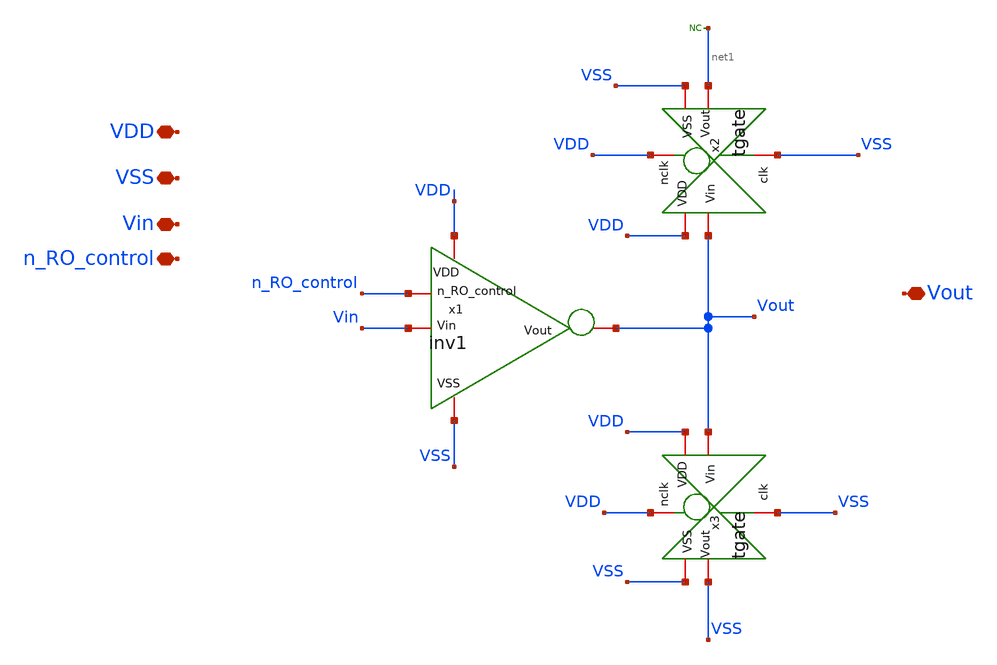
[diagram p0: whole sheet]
** sch_path: TT/rovcel4.sch
**.subckt rovcel4 VDD VSS Vin n_RO_control Vout
*.iopin VDD
*.iopin VSS
*.iopin Vin
*.iopin n_RO_control
*.iopin Vout
x1 n_RO_control VDD VSS Vin Vout inv1
x2 VDD VDD Vout net1 VSS VSS tgate
x3 VDD VDD Vout VSS VSS VSS tgate
* noconn #net1
**.ends

* expanding   symbol:  /foss/designs/Projects/RO_reliability/xschem/inv1.sym # of pins=5
** sym_path: TT/inv1.sym
** sch_path: TT/inv1.sch
.subckt inv1 n_RO_control VDD VSS Vin Vout
*.iopin VDD
*.iopin VSS
*.iopin Vin
*.iopin Vout
*.iopin n_RO_control
XM1 net1 n_RO_control VDD VDD sky130_fd_pr__pfet_01v8 L=0.15 W=4.75 nf=1 ad='int((nf+1)/2) * W/nf * 0.29'
+ as='int((nf+2)/2) * W/nf * 0.29' pd='2*int((nf+1)/2) * (W/nf + 0.29)' ps='2*int((nf+2)/2) * (W/nf + 0.29)'
+ nrd='0.29 / W' nrs='0.29 / W' sa=0 sb=0 sd=0 mult=40 m=40
XM2 Vout Vin net1 VDD sky130_fd_pr__pfet_01v8 L=0.15 W=4.75 nf=1 ad='int((nf+1)/2) * W/nf * 0.29' as='int((nf+2)/2) * W/nf * 0.29'
+ pd='2*int((nf+1)/2) * (W/nf + 0.29)' ps='2*int((nf+2)/2) * (W/nf + 0.29)' nrd='0.29 / W' nrs='0.29 / W'
+ sa=0 sb=0 sd=0 mult=4 m=4
XM3 Vout Vin VSS VSS sky130_fd_pr__nfet_01v8 L=0.15 W=2.1 nf=1 ad='int((nf+1)/2) * W/nf * 0.29' as='int((nf+2)/2) * W/nf * 0.29'
+ pd='2*int((nf+1)/2) * (W/nf + 0.29)' ps='2*int((nf+2)/2) * (W/nf + 0.29)' nrd='0.29 / W' nrs='0.29 / W'
+ sa=0 sb=0 sd=0 mult=2 m=2
.ends


* expanding   symbol:  /foss/designs/Projects/RO_reliability/xschem/tgate.sym # of pins=6
** sym_path: TT/tgate.sym
** sch_path: TT/tgate.sch
.subckt tgate nclk VDD Vin Vout VSS clk
*.iopin nclk
*.iopin clk
*.iopin VDD
*.iopin VSS
*.iopin Vout
*.iopin Vin
XM1 Vin nclk Vout VDD sky130_fd_pr__pfet_01v8 L=0.15 W=0.45 nf=1 ad='int((nf+1)/2) * W/nf * 0.29' as='int((nf+2)/2) * W/nf * 0.29'
+ pd='2*int((nf+1)/2) * (W/nf + 0.29)' ps='2*int((nf+2)/2) * (W/nf + 0.29)' nrd='0.29 / W' nrs='0.29 / W'
+ sa=0 sb=0 sd=0 mult=1 m=1
XM2 Vin clk Vout VSS sky130_fd_pr__nfet_01v8 L=0.15 W=0.45 nf=1 ad='int((nf+1)/2) * W/nf * 0.29' as='int((nf+2)/2) * W/nf * 0.29'
+ pd='2*int((nf+1)/2) * (W/nf + 0.29)' ps='2*int((nf+2)/2) * (W/nf + 0.29)' nrd='0.29 / W' nrs='0.29 / W'
+ sa=0 sb=0 sd=0 mult=1 m=1
.ends

.end
